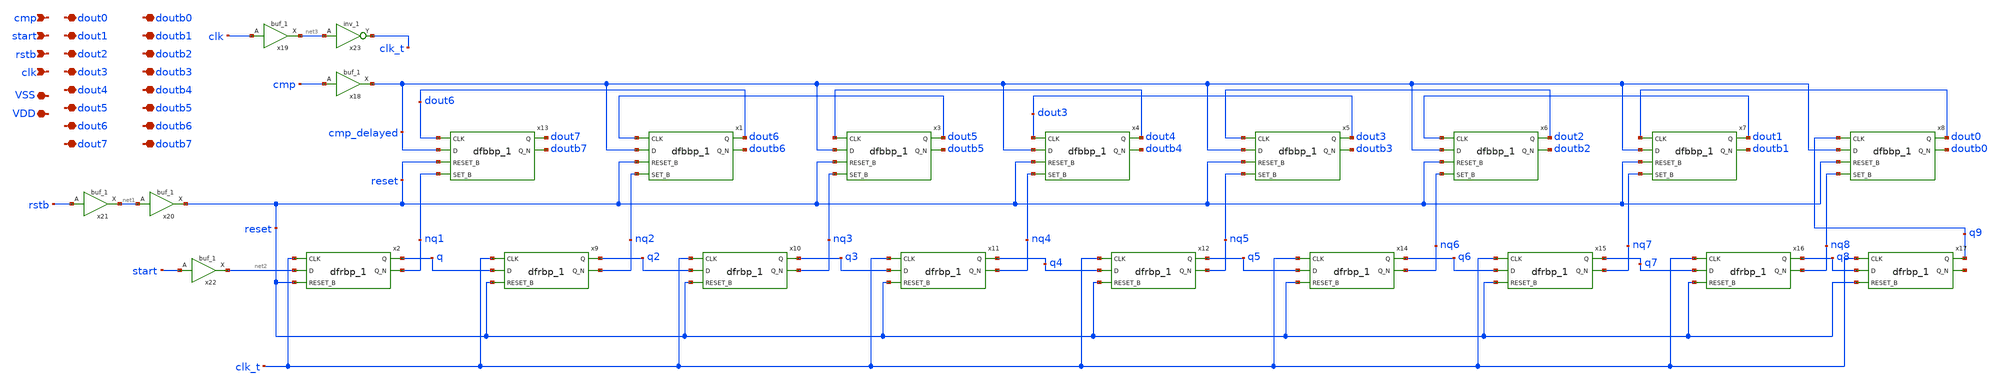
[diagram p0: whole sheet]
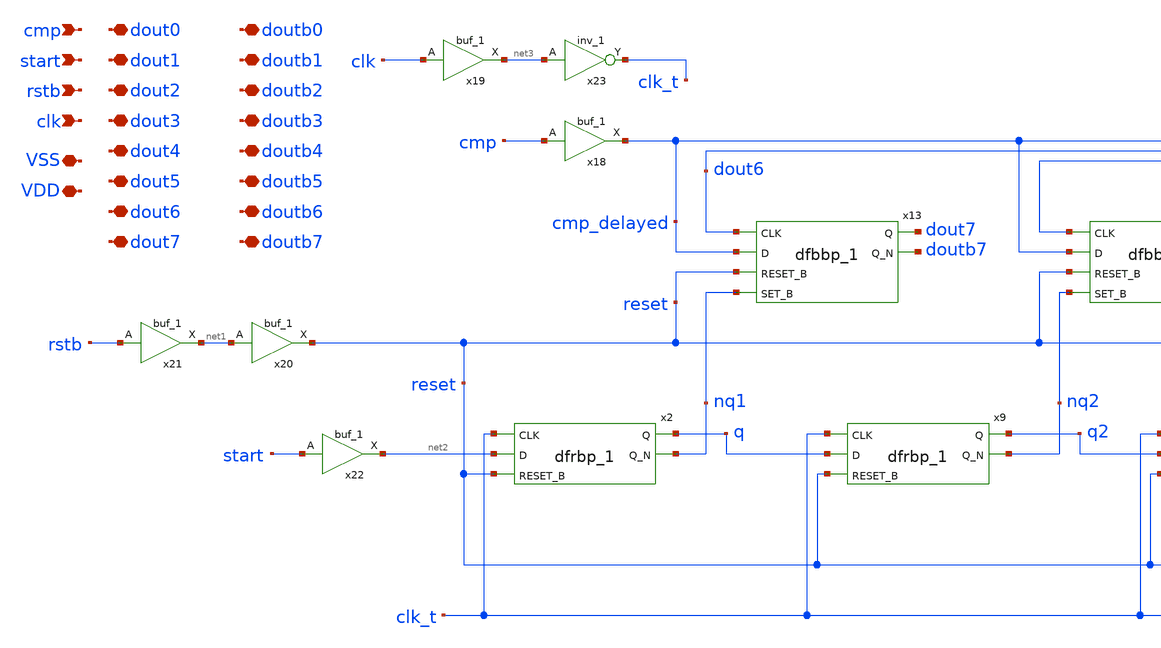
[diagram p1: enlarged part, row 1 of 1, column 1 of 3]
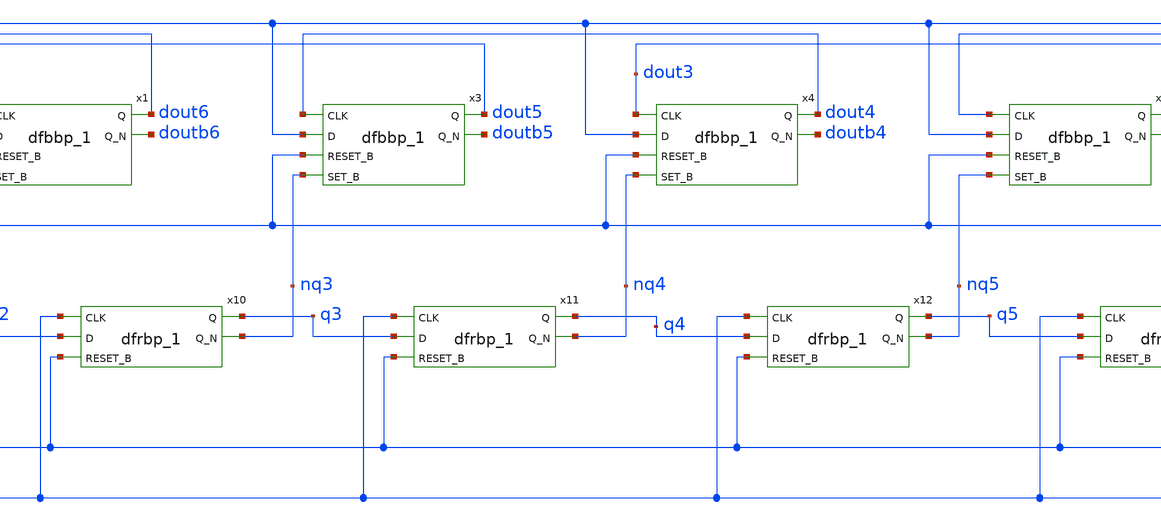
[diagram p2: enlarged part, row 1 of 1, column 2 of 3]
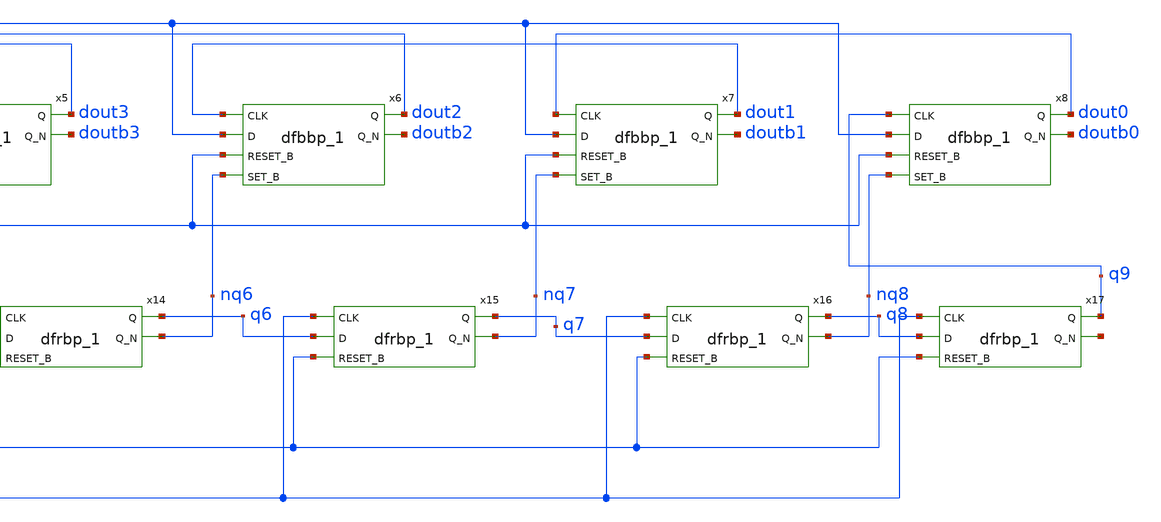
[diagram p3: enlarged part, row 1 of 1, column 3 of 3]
** sch_path: 8bitADC_SARLOGIC_pinout.sch
**.subckt 8bitADC_SARLOGIC_pinout cmp start rstb clk dout0 doutb0 VSS VDD dout1 dout2 dout3 dout4
*+ dout5 dout6 dout7 doutb1 doutb2 doutb3 doutb4 doutb5 doutb6 doutb7
*.ipin cmp
*.ipin start
*.ipin rstb
*.ipin clk
*.iopin dout0
*.iopin doutb0
*.iopin VSS
*.iopin VDD
*.iopin dout1
*.iopin dout2
*.iopin dout3
*.iopin dout4
*.iopin dout5
*.iopin dout6
*.iopin dout7
*.iopin doutb1
*.iopin doutb2
*.iopin doutb3
*.iopin doutb4
*.iopin doutb5
*.iopin doutb6
*.iopin doutb7
x18 cmp VSS VNB VPB VDD cmp_delayed sky130_fd_sc_hd__buf_1
x19 clk VSS VNB VPB VDD net3 sky130_fd_sc_hd__buf_1
x20 net1 VSS VNB VPB VDD reset sky130_fd_sc_hd__buf_1
x21 rstb VSS VNB VPB VDD net1 sky130_fd_sc_hd__buf_1
x22 start VSS VNB VPB VDD net2 sky130_fd_sc_hd__buf_1
x2 clk_t net2 reset VSS VNB VPB VDD q nq1 sky130_fd_sc_hd__dfrbp_1
x9 clk_t q reset VSS VNB VPB VDD q2 nq2 sky130_fd_sc_hd__dfrbp_1
x10 clk_t q2 reset VSS VNB VPB VDD q3 nq3 sky130_fd_sc_hd__dfrbp_1
x11 clk_t q3 reset VSS VNB VPB VDD q4 nq4 sky130_fd_sc_hd__dfrbp_1
x12 clk_t q4 reset VSS VNB VPB VDD q5 nq5 sky130_fd_sc_hd__dfrbp_1
x14 clk_t q5 reset VSS VNB VPB VDD q6 nq6 sky130_fd_sc_hd__dfrbp_1
x15 clk_t q6 reset VSS VNB VPB VDD q7 nq7 sky130_fd_sc_hd__dfrbp_1
x16 clk_t q7 reset VSS VNB VPB VDD q8 nq8 sky130_fd_sc_hd__dfrbp_1
x17 clk_t q8 reset VSS VNB VPB VDD q9 net4 sky130_fd_sc_hd__dfrbp_1
x23 net3 VSS VNB VPB VDD clk_t sky130_fd_sc_hd__inv_1
x13 dout6 cmp_delayed reset nq1 VSS VNB VPB VDD dout7 doutb7 sky130_fd_sc_hd__dfbbp_1
x1 dout5 cmp_delayed reset nq2 VSS VNB VPB VDD dout6 doutb6 sky130_fd_sc_hd__dfbbp_1
x3 dout4 cmp_delayed reset nq3 VSS VNB VPB VDD dout5 doutb5 sky130_fd_sc_hd__dfbbp_1
x4 dout3 cmp_delayed reset nq4 VSS VNB VPB VDD dout4 doutb4 sky130_fd_sc_hd__dfbbp_1
x5 dout2 cmp_delayed reset nq5 VSS VNB VPB VDD dout3 doutb3 sky130_fd_sc_hd__dfbbp_1
x6 dout1 cmp_delayed reset nq6 VSS VNB VPB VDD dout2 doutb2 sky130_fd_sc_hd__dfbbp_1
x7 dout0 cmp_delayed reset nq7 VSS VNB VPB VDD dout1 doutb1 sky130_fd_sc_hd__dfbbp_1
x8 q9 cmp_delayed reset nq8 VSS VNB VPB VDD dout0 doutb0 sky130_fd_sc_hd__dfbbp_1
**.ends
.end
